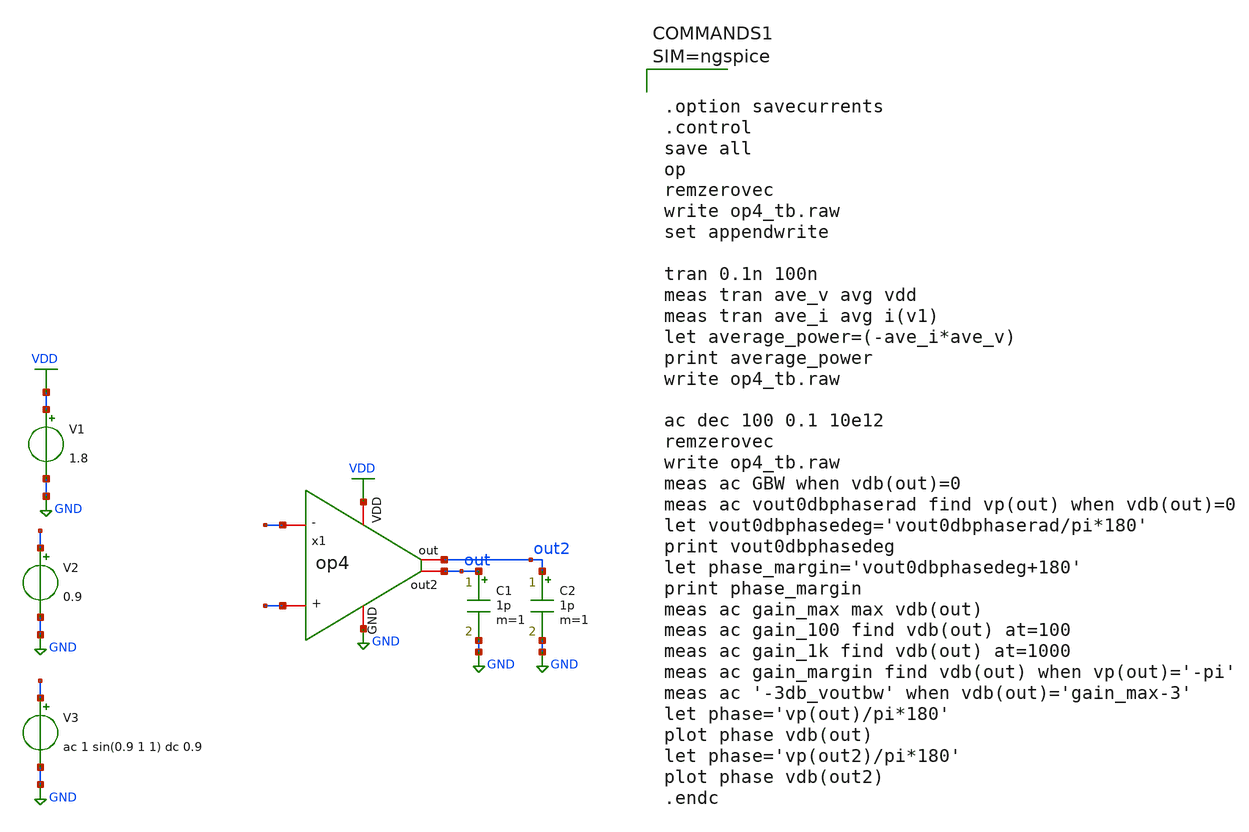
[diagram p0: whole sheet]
** sch_path: xschem/op4_tb.sch
**.subckt op4_tb
V1 VDD GND 1.8
V2 - GND 0.9
V3 + GND ac 1 sin(0.9 1 1) dc 0.9
C1 out GND 1p m=1
x1 VDD out2 out - + GND op4
C2 out2 GND 1p m=1
**** begin user architecture code

** opencircuitdesign pdks install
.lib $::SKYWATER_MODELS/sky130.lib.spice tt





.option savecurrents
.control
save all
op
remzerovec
write op4_tb.raw
set appendwrite

tran 0.1n 100n
meas tran ave_v avg vdd
meas tran ave_i avg i(v1)
let average_power=(-ave_i*ave_v)
print average_power
write op4_tb.raw

ac dec 100 0.1 10e12
remzerovec
write op4_tb.raw
meas ac GBW when vdb(out)=0
meas ac vout0dbphaserad find vp(out) when vdb(out)=0
let vout0dbphasedeg='vout0dbphaserad/pi*180'
print vout0dbphasedeg
let phase_margin='vout0dbphasedeg+180'
print phase_margin
meas ac gain_max max vdb(out)
meas ac gain_100 find vdb(out) at=100
meas ac gain_1k find vdb(out) at=1000
meas ac gain_margin find vdb(out) when vp(out)='-pi'
meas ac '-3db_voutbw' when vdb(out)='gain_max-3'
let phase='vp(out)/pi*180'
plot phase vdb(out)
let phase='vp(out2)/pi*180'
plot phase vdb(out2)
.endc



**** end user architecture code
**.ends

* expanding   symbol:  op4.sym # of pins=6
** sym_path: xschem/op4.sym
** sch_path: xschem/op4.sch
.subckt op4 VDD out out2 - + GND
*.iopin VDD
*.iopin GND
*.iopin -
*.iopin +
*.iopin out
*.iopin out2
C2 out2 net4 1p m=1
R2 net4 out 1k m=1
XM1 bias bias net5 GND sky130_fd_pr__nfet_01v8 L={L5} W={W5} nf=1 ad='int((nf+1)/2) * W/nf * 0.29' as='int((nf+2)/2) * W/nf * 0.29'
+ pd='2*int((nf+1)/2) * (W/nf + 0.29)' ps='2*int((nf+2)/2) * (W/nf + 0.29)' nrd='0.29 / W' nrs='0.29 / W'
+ sa=0 sb=0 sd=0 mult=2 m=2
XM2 net3 bias GND GND sky130_fd_pr__nfet_01v8 L={L5} W={W5} nf=1 ad='int((nf+1)/2) * W/nf * 0.29' as='int((nf+2)/2) * W/nf * 0.29'
+ pd='2*int((nf+1)/2) * (W/nf + 0.29)' ps='2*int((nf+2)/2) * (W/nf + 0.29)' nrd='0.29 / W' nrs='0.29 / W'
+ sa=0 sb=0 sd=0 mult=2 m=2
XM3 net1 - net2 GND sky130_fd_pr__nfet_01v8 L={L4} W={W4} nf=1 ad='int((nf+1)/2) * W/nf * 0.29' as='int((nf+2)/2) * W/nf * 0.29'
+ pd='2*int((nf+1)/2) * (W/nf + 0.29)' ps='2*int((nf+2)/2) * (W/nf + 0.29)' nrd='0.29 / W' nrs='0.29 / W'
+ sa=0 sb=0 sd=0 mult=2 m=2
XM4 out + net2 GND sky130_fd_pr__nfet_01v8 L={L4} W={W4} nf=1 ad='int((nf+1)/2) * W/nf * 0.29' as='int((nf+2)/2) * W/nf * 0.29'
+ pd='2*int((nf+1)/2) * (W/nf + 0.29)' ps='2*int((nf+2)/2) * (W/nf + 0.29)' nrd='0.29 / W' nrs='0.29 / W'
+ sa=0 sb=0 sd=0 mult=2 m=2
XM6 bias net3 VDD VDD sky130_fd_pr__pfet_01v8 L={L1} W={W1} nf=1 ad='int((nf+1)/2) * W/nf * 0.29' as='int((nf+2)/2) * W/nf * 0.29'
+ pd='2*int((nf+1)/2) * (W/nf + 0.29)' ps='2*int((nf+2)/2) * (W/nf + 0.29)' nrd='0.29 / W' nrs='0.29 / W'
+ sa=0 sb=0 sd=0 mult=2 m=2
XM7 net3 net3 VDD VDD sky130_fd_pr__pfet_01v8 L={L1} W={W1} nf=1 ad='int((nf+1)/2) * W/nf * 0.29' as='int((nf+2)/2) * W/nf * 0.29'
+ pd='2*int((nf+1)/2) * (W/nf + 0.29)' ps='2*int((nf+2)/2) * (W/nf + 0.29)' nrd='0.29 / W' nrs='0.29 / W'
+ sa=0 sb=0 sd=0 mult=2 m=2
XM8 out net1 VDD VDD sky130_fd_pr__pfet_01v8 L={L7} W={W7} nf=1 ad='int((nf+1)/2) * W/nf * 0.29' as='int((nf+2)/2) * W/nf * 0.29'
+ pd='2*int((nf+1)/2) * (W/nf + 0.29)' ps='2*int((nf+2)/2) * (W/nf + 0.29)' nrd='0.29 / W' nrs='0.29 / W'
+ sa=0 sb=0 sd=0 mult=4 m=4
XM9 net1 net1 VDD VDD sky130_fd_pr__pfet_01v8 L={L7} W={W7} nf=1 ad='int((nf+1)/2) * W/nf * 0.29' as='int((nf+2)/2) * W/nf * 0.29'
+ pd='2*int((nf+1)/2) * (W/nf + 0.29)' ps='2*int((nf+2)/2) * (W/nf + 0.29)' nrd='0.29 / W' nrs='0.29 / W'
+ sa=0 sb=0 sd=0 mult=4 m=4
XM5 net2 bias GND GND sky130_fd_pr__nfet_01v8 L={L6} W={W6} nf=1 ad='int((nf+1)/2) * W/nf * 0.29' as='int((nf+2)/2) * W/nf * 0.29'
+ pd='2*int((nf+1)/2) * (W/nf + 0.29)' ps='2*int((nf+2)/2) * (W/nf + 0.29)' nrd='0.29 / W' nrs='0.29 / W'
+ sa=0 sb=0 sd=0 mult=2 m=2
XM10 out2 out VDD VDD sky130_fd_pr__pfet_01v8 L={L2} W={W2} nf=1 ad='int((nf+1)/2) * W/nf * 0.29' as='int((nf+2)/2) * W/nf * 0.29'
+ pd='2*int((nf+1)/2) * (W/nf + 0.29)' ps='2*int((nf+2)/2) * (W/nf + 0.29)' nrd='0.29 / W' nrs='0.29 / W'
+ sa=0 sb=0 sd=0 mult=4 m=4
XM11 out2 bias GND GND sky130_fd_pr__nfet_01v8 L={L3} W={W3} nf=1 ad='int((nf+1)/2) * W/nf * 0.29' as='int((nf+2)/2) * W/nf * 0.29'
+ pd='2*int((nf+1)/2) * (W/nf + 0.29)' ps='2*int((nf+2)/2) * (W/nf + 0.29)' nrd='0.29 / W' nrs='0.29 / W'
+ sa=0 sb=0 sd=0 mult=2 m=2
R3 net5 GND 4.5k m=1
**** begin user architecture code


**************
*PMOS cms
.param L1=40
.param W1=1

**************
*NMOS cms
.param L5=20
.param W5=1

**************
*PMOS differential
.param L7=10
.param W7=0.5

**************
*differential Pair
.param L4=10
.param W4=1.5

**************
*NMOS current control
.param L6=5
.param W6=1

**************
*Second Stage
.param L2=30
.param W2=1

**************
*NMOS current second stage
.param L3=20
.param W3=0.5


**** end user architecture code
.ends

.GLOBAL VDD
.GLOBAL GND
.end
